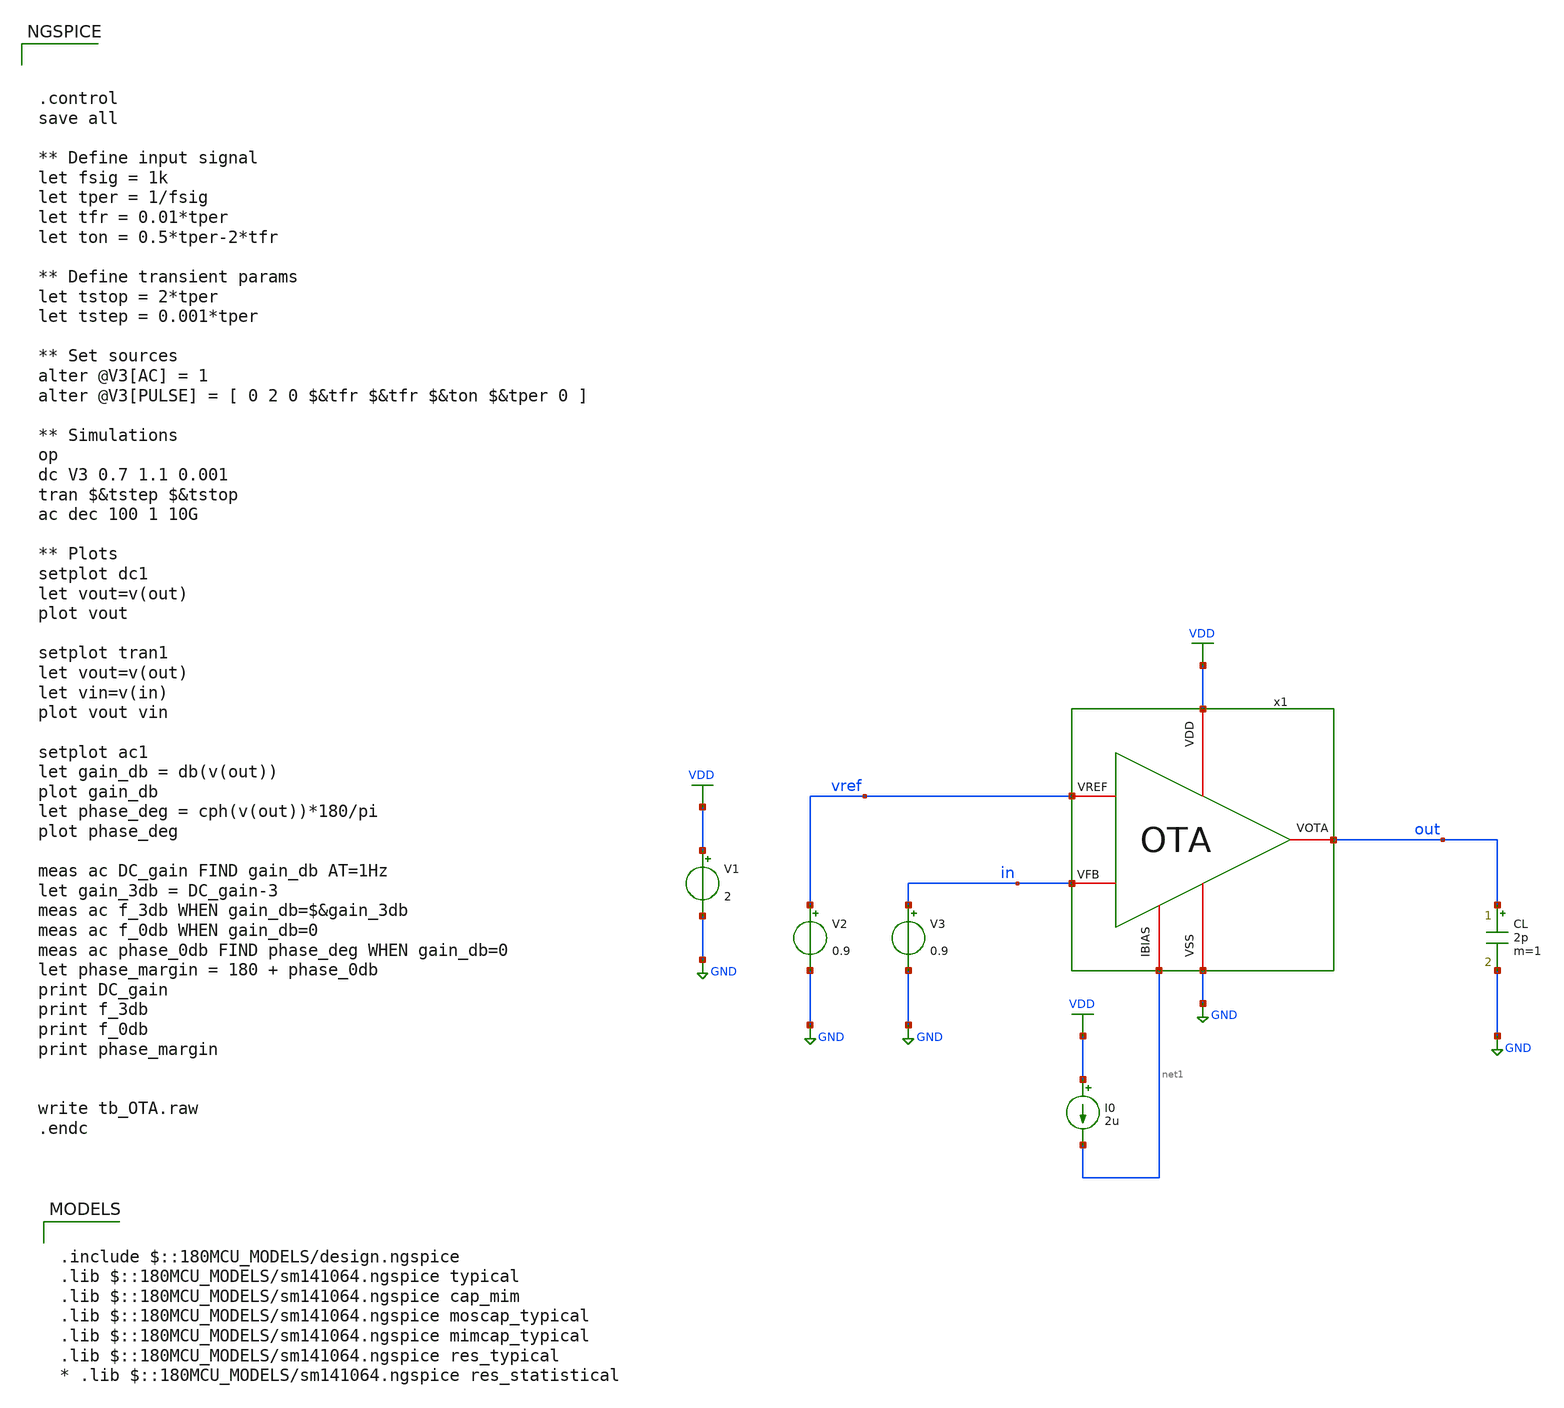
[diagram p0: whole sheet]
** sch_path: designs/libs/tb_ldo/tb_ldo/tb_ldo_OTA/tb_OTA.sch
**.subckt tb_OTA
V1 VDD GND 2
V2 vref GND 0.9
I0 VDD net1 2u
CL out GND 2p m=1
V3 in GND 0.9
x1 VDD vref in out net1 GND OTA
**** begin user architecture code

.include $::180MCU_MODELS/design.ngspice
.lib $::180MCU_MODELS/sm141064.ngspice typical
.lib $::180MCU_MODELS/sm141064.ngspice cap_mim
.lib $::180MCU_MODELS/sm141064.ngspice moscap_typical
.lib $::180MCU_MODELS/sm141064.ngspice mimcap_typical
.lib $::180MCU_MODELS/sm141064.ngspice res_typical
* .lib $::180MCU_MODELS/sm141064.ngspice res_statistical




.control
save all

** Define input signal
let fsig = 1k
let tper = 1/fsig
let tfr = 0.01*tper
let ton = 0.5*tper-2*tfr

** Define transient params
let tstop = 2*tper
let tstep = 0.001*tper

** Set sources
alter @V3[AC] = 1
alter @V3[PULSE] = [ 0 2 0 $&tfr $&tfr $&ton $&tper 0 ]

** Simulations
op
dc V3 0.7 1.1 0.001
tran $&tstep $&tstop
ac dec 100 1 10G

** Plots
setplot dc1
let vout=v(out)
plot vout

setplot tran1
let vout=v(out)
let vin=v(in)
plot vout vin

setplot ac1
let gain_db = db(v(out))
plot gain_db
let phase_deg = cph(v(out))*180/pi
plot phase_deg

meas ac DC_gain FIND gain_db AT=1Hz
let gain_3db = DC_gain-3
meas ac f_3db WHEN gain_db=$&gain_3db
meas ac f_0db WHEN gain_db=0
meas ac phase_0db FIND phase_deg WHEN gain_db=0
let phase_margin = 180 + phase_0db
print DC_gain
print f_3db
print f_0db
print phase_margin


write tb_OTA.raw
.endc


**** end user architecture code
**.ends

* expanding   symbol:  libs/core_ldo/ldo/ldo_OTA/OTA.sym # of pins=6
** sym_path: designs/libs/core_ldo/ldo/OTA.sym
** sch_path: designs/libs/core_ldo/ldo/OTA.sch
.subckt OTA VDD VREF VFB VOTA IBIAS VSS
*.iopin VDD
*.iopin VSS
*.iopin VOTA
*.iopin VREF
*.iopin IBIAS
*.iopin VFB
XM3 net2 net2 VDD VDD pfet_05v0 L=2.00u W=8.00u nf=1 ad='int((nf+1)/2) * W/nf * 0.18u' as='int((nf+2)/2) * W/nf * 0.18u'
+ pd='2*int((nf+1)/2) * (W/nf + 0.18u)' ps='2*int((nf+2)/2) * (W/nf + 0.18u)' nrd='0.18u / W' nrs='0.18u / W'
+ sa=0 sb=0 sd=0 m=1
XM4 net3 net3 VDD VDD pfet_05v0 L=2.00u W=8.00u nf=1 ad='int((nf+1)/2) * W/nf * 0.18u' as='int((nf+2)/2) * W/nf * 0.18u'
+ pd='2*int((nf+1)/2) * (W/nf + 0.18u)' ps='2*int((nf+2)/2) * (W/nf + 0.18u)' nrd='0.18u / W' nrs='0.18u / W'
+ sa=0 sb=0 sd=0 m=1
XM5 net4 net2 VDD VDD pfet_05v0 L=2.00u W=8.00u nf=1 ad='int((nf+1)/2) * W/nf * 0.18u' as='int((nf+2)/2) * W/nf * 0.18u'
+ pd='2*int((nf+1)/2) * (W/nf + 0.18u)' ps='2*int((nf+2)/2) * (W/nf + 0.18u)' nrd='0.18u / W' nrs='0.18u / W'
+ sa=0 sb=0 sd=0 m=1
XM6 VOTA net3 VDD VDD pfet_05v0 L=2.00u W=8.00u nf=1 ad='int((nf+1)/2) * W/nf * 0.18u' as='int((nf+2)/2) * W/nf * 0.18u'
+ pd='2*int((nf+1)/2) * (W/nf + 0.18u)' ps='2*int((nf+2)/2) * (W/nf + 0.18u)' nrd='0.18u / W' nrs='0.18u / W'
+ sa=0 sb=0 sd=0 m=2
XM9 IBIAS IBIAS VSS VSS nfet_05v0 L=2.00u W=4.00u nf=1 ad='int((nf+1)/2) * W/nf * 0.18u' as='int((nf+2)/2) * W/nf * 0.18u'
+ pd='2*int((nf+1)/2) * (W/nf + 0.18u)' ps='2*int((nf+2)/2) * (W/nf + 0.18u)' nrd='0.18u / W' nrs='0.18u / W'
+ sa=0 sb=0 sd=0 m=1
XM10 net1 IBIAS VSS VSS nfet_05v0 L=2.00u W=4.00u nf=1 ad='int((nf+1)/2) * W/nf * 0.18u' as='int((nf+2)/2) * W/nf * 0.18u'
+ pd='2*int((nf+1)/2) * (W/nf + 0.18u)' ps='2*int((nf+2)/2) * (W/nf + 0.18u)' nrd='0.18u / W' nrs='0.18u / W'
+ sa=0 sb=0 sd=0 m=1
XM7 net4 net4 VSS VSS nfet_05v0 L=2.00u W=4.00u nf=1 ad='int((nf+1)/2) * W/nf * 0.18u' as='int((nf+2)/2) * W/nf * 0.18u'
+ pd='2*int((nf+1)/2) * (W/nf + 0.18u)' ps='2*int((nf+2)/2) * (W/nf + 0.18u)' nrd='0.18u / W' nrs='0.18u / W'
+ sa=0 sb=0 sd=0 m=1
XM8 VOTA net4 VSS VSS nfet_05v0 L=2.00u W=4.00u nf=1 ad='int((nf+1)/2) * W/nf * 0.18u' as='int((nf+2)/2) * W/nf * 0.18u'
+ pd='2*int((nf+1)/2) * (W/nf + 0.18u)' ps='2*int((nf+2)/2) * (W/nf + 0.18u)' nrd='0.18u / W' nrs='0.18u / W'
+ sa=0 sb=0 sd=0 m=2
XM1 net2 VREF net1 net1 nfet_05v0 L=0.60u W=40.00u nf=1 ad='int((nf+1)/2) * W/nf * 0.18u' as='int((nf+2)/2) * W/nf * 0.18u'
+ pd='2*int((nf+1)/2) * (W/nf + 0.18u)' ps='2*int((nf+2)/2) * (W/nf + 0.18u)' nrd='0.18u / W' nrs='0.18u / W'
+ sa=0 sb=0 sd=0 m=1
XM2 net3 VFB net1 net1 nfet_05v0 L=0.60u W=40.00u nf=1 ad='int((nf+1)/2) * W/nf * 0.18u' as='int((nf+2)/2) * W/nf * 0.18u'
+ pd='2*int((nf+1)/2) * (W/nf + 0.18u)' ps='2*int((nf+2)/2) * (W/nf + 0.18u)' nrd='0.18u / W' nrs='0.18u / W'
+ sa=0 sb=0 sd=0 m=1
.ends

.GLOBAL GND
.GLOBAL VDD
.end
